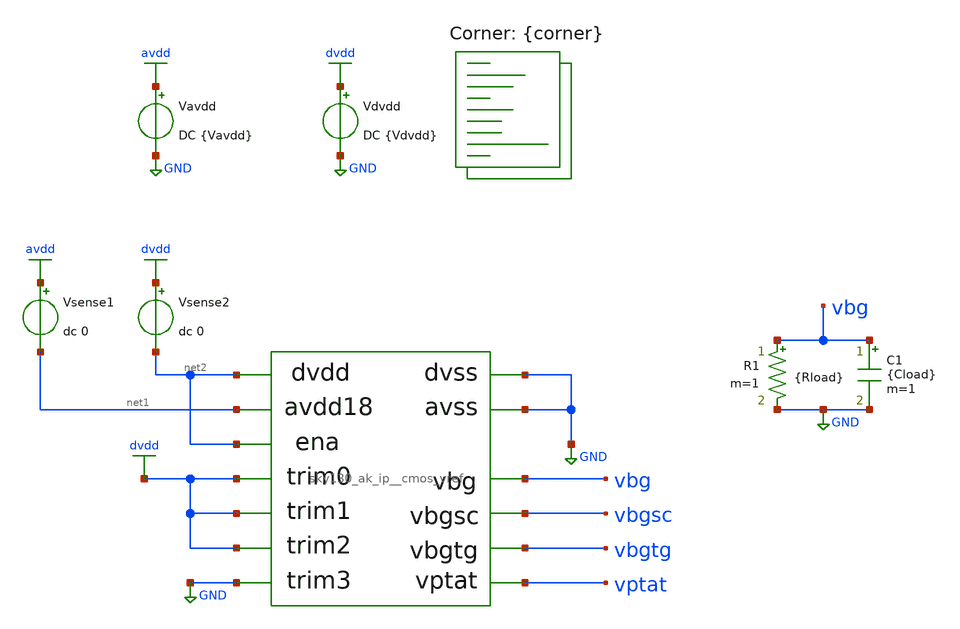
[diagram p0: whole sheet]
** sch_path: cace/tb_temp_sweep.sch
**.subckt tb_temp_sweep
Vavdd avdd GND DC {Vavdd}
X1 net1 GND dvdd vbg vptat dvdd dvdd GND net2 GND net2 vbgsc vbgtg sky130_ak_ip__cmos_vref
Vsense1 avdd net1 dc 0
Vdvdd dvdd GND DC {Vdvdd}
C1 vbg GND {Cload} m=1
Vsense2 dvdd net2 dc 0
R1 vbg GND {Rload} m=1
**** begin user architecture code


.option warn=1
.nodeset v(vbg)=1.2
.nodeset v(vptat)=0.1
.control
save vbg
dc TEMP {temperature|minimum} {temperature|maximum} 5
set wr_singlescale
wrdata {simpath}/{filename}_{N}.data V(vbg)
quit
.endc


.lib $::SKYWATER_MODELS/sky130.lib.spice {corner}
 .include $::SKYWATER_STDCELLS/sky130_fd_sc_hd.spice
**** end user architecture code
**.ends
.GLOBAL avdd
.GLOBAL GND
.GLOBAL dvdd
.end
